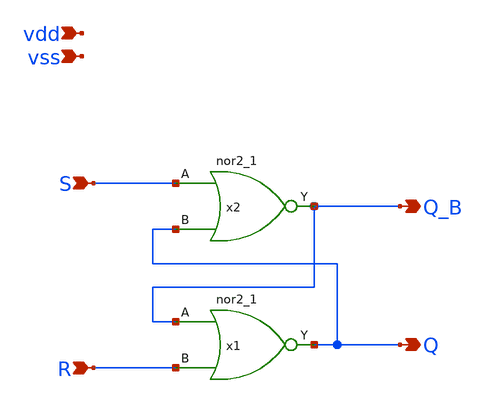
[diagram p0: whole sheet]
** sch_path: xschem/srlatch.sch
**.subckt srlatch S R Q_B Q vdd vss
*.ipin S
*.ipin R
*.opin Q_B
*.opin Q
*.ipin vdd
*.ipin vss
x2 S Q vss vss vdd vdd Q_B sky130_fd_sc_hd__nor2_1
x1 Q_B R vss vss vdd vdd Q sky130_fd_sc_hd__nor2_1
**.ends
.end
